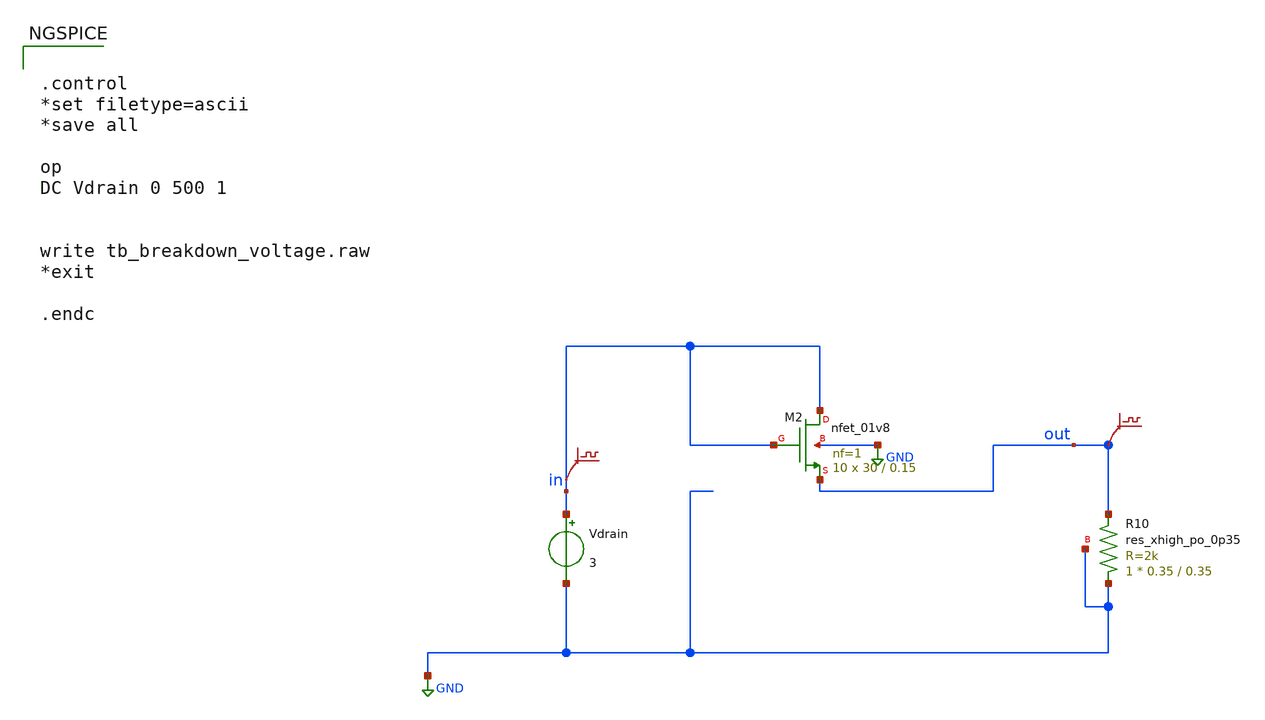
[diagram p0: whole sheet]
** sch_path: xschem/breakdown_voltage_tb.sch
**.subckt breakdown_voltage_tb
.save v(in)
.save v(out)
XM2 in in out GND sky130_fd_pr__nfet_01v8 L=0.15 W=30 nf=1 ad='int((1 + 1)/2) * 30 / 1 * 0.29' as='int((1 + 2)/2) * 30 / 1 * 0.29'
+ pd='2*int((1 + 1)/2) * (30 / 1 + 0.29)' ps='2*int((1 + 2)/2) * (30 / 1 + 0.29)' nrd='0.29 / 30 ' nrs='0.29 / 30 '
+ sa=0 sb=0 sd=0 mult=10 m=10
Vdrain in GND 3
XR10 GND out GND sky130_fd_pr__res_xhigh_po_0p35 L=0.35 mult=1 m=1
**** begin user architecture code


.control
*set filetype=ascii
*save all

op
DC Vdrain 0 500 1


write tb_breakdown_voltage.raw
*exit

.endc



** opencircuitdesign pdks install
.lib $::SKYWATER_MODELS/sky130.lib.spice tt


**** end user architecture code
**.ends
.GLOBAL GND
.end
